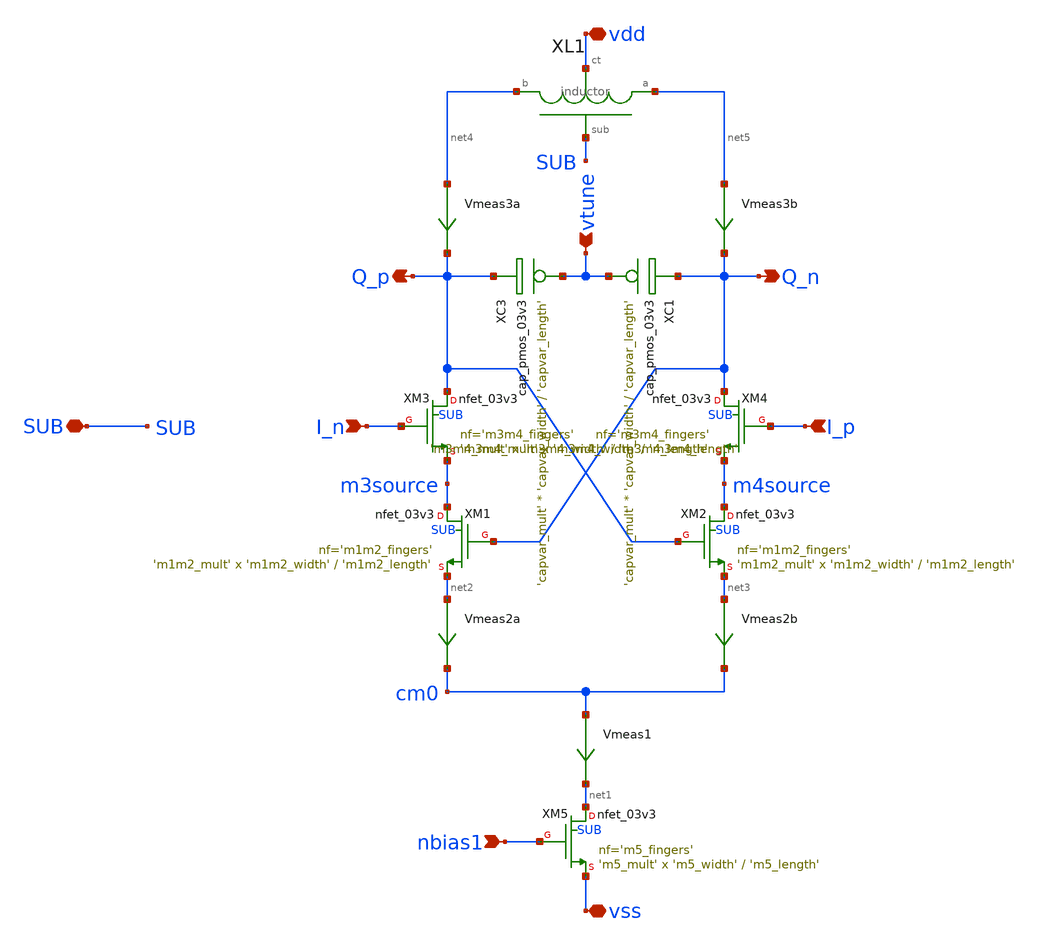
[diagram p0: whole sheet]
** sch_path: sch/vco/half_qvco_cell.sch
**.subckt half_qvco_cell SUB vdd vss I_n nbias1 Q_p Q_n I_p vtune
*.iopin SUB
*.iopin vdd
*.iopin vss
*.ipin I_n
*.ipin nbias1
*.opin Q_p
*.opin Q_n
*.ipin I_p
*.ipin vtune
XL1 vdd net5 SUB net4 inductor
XM5 net1 nbias1 vss SUB nfet_03v3 L='m5_length' W='m5_width' nf='m5_fingers' ad='int((nf+1)/2) * W/nf * 0.18u'
+ as='int((nf+2)/2) * W/nf * 0.18u' pd='2*int((nf+1)/2) * (W/nf + 0.18u)' ps='2*int((nf+2)/2) * (W/nf + 0.18u)'
+ nrd='0.18u / W' nrs='0.18u / W' sa=0 sb=0 sd=0 m='m5_mult' par='m5_mult'
Vmeas1 cm0 net1 0
.save i(vmeas1)
Vmeas2a net2 cm0 0
.save i(vmeas2a)
Vmeas2b net3 cm0 0
.save i(vmeas2b)
Vmeas3a net4 Q_p 0
.save i(vmeas3a)
Vmeas3b net5 Q_n 0
.save i(vmeas3b)
XM1 m3source Q_n net2 SUB nfet_03v3 L='m1m2_length' W='m1m2_width' nf='m1m2_fingers' ad='int((nf+1)/2) * W/nf * 0.18u'
+ as='int((nf+2)/2) * W/nf * 0.18u' pd='2*int((nf+1)/2) * (W/nf + 0.18u)' ps='2*int((nf+2)/2) * (W/nf + 0.18u)'
+ nrd='0.18u / W' nrs='0.18u / W' sa=0 sb=0 sd=0 m='m1m2_mult' par='m1m2_mult'
XM2 m4source Q_p net3 SUB nfet_03v3 L='m1m2_length' W='m1m2_width' nf='m1m2_fingers' ad='int((nf+1)/2) * W/nf * 0.18u'
+ as='int((nf+2)/2) * W/nf * 0.18u' pd='2*int((nf+1)/2) * (W/nf + 0.18u)' ps='2*int((nf+2)/2) * (W/nf + 0.18u)'
+ nrd='0.18u / W' nrs='0.18u / W' sa=0 sb=0 sd=0 m='m1m2_mult' par='m1m2_mult'
XM3 Q_p I_n m3source SUB nfet_03v3 L='m3m4_length' W='m3m4_width' nf='m3m4_fingers' ad='int((nf+1)/2) * W/nf * 0.18u'
+ as='int((nf+2)/2) * W/nf * 0.18u' pd='2*int((nf+1)/2) * (W/nf + 0.18u)' ps='2*int((nf+2)/2) * (W/nf + 0.18u)'
+ nrd='0.18u / W' nrs='0.18u / W' sa=0 sb=0 sd=0 m='m3m4_mult' par='m3m4_mult'
XM4 Q_n I_p m4source SUB nfet_03v3 L='m3m4_length' W='m3m4_width' nf='m3m4_fingers' ad='int((nf+1)/2) * W/nf * 0.18u'
+ as='int((nf+2)/2) * W/nf * 0.18u' pd='2*int((nf+1)/2) * (W/nf + 0.18u)' ps='2*int((nf+2)/2) * (W/nf + 0.18u)'
+ nrd='0.18u / W' nrs='0.18u / W' sa=0 sb=0 sd=0 m='m3m4_mult' par='m3m4_mult'
XC1 vtune Q_n cap_pmos_03v3 c_width='capvar_width' c_length='capvar_length' m='capvar_mult'
XC3 vtune Q_p cap_pmos_03v3 c_width='capvar_width' c_length='capvar_length' m='capvar_mult'
**.ends
.end
